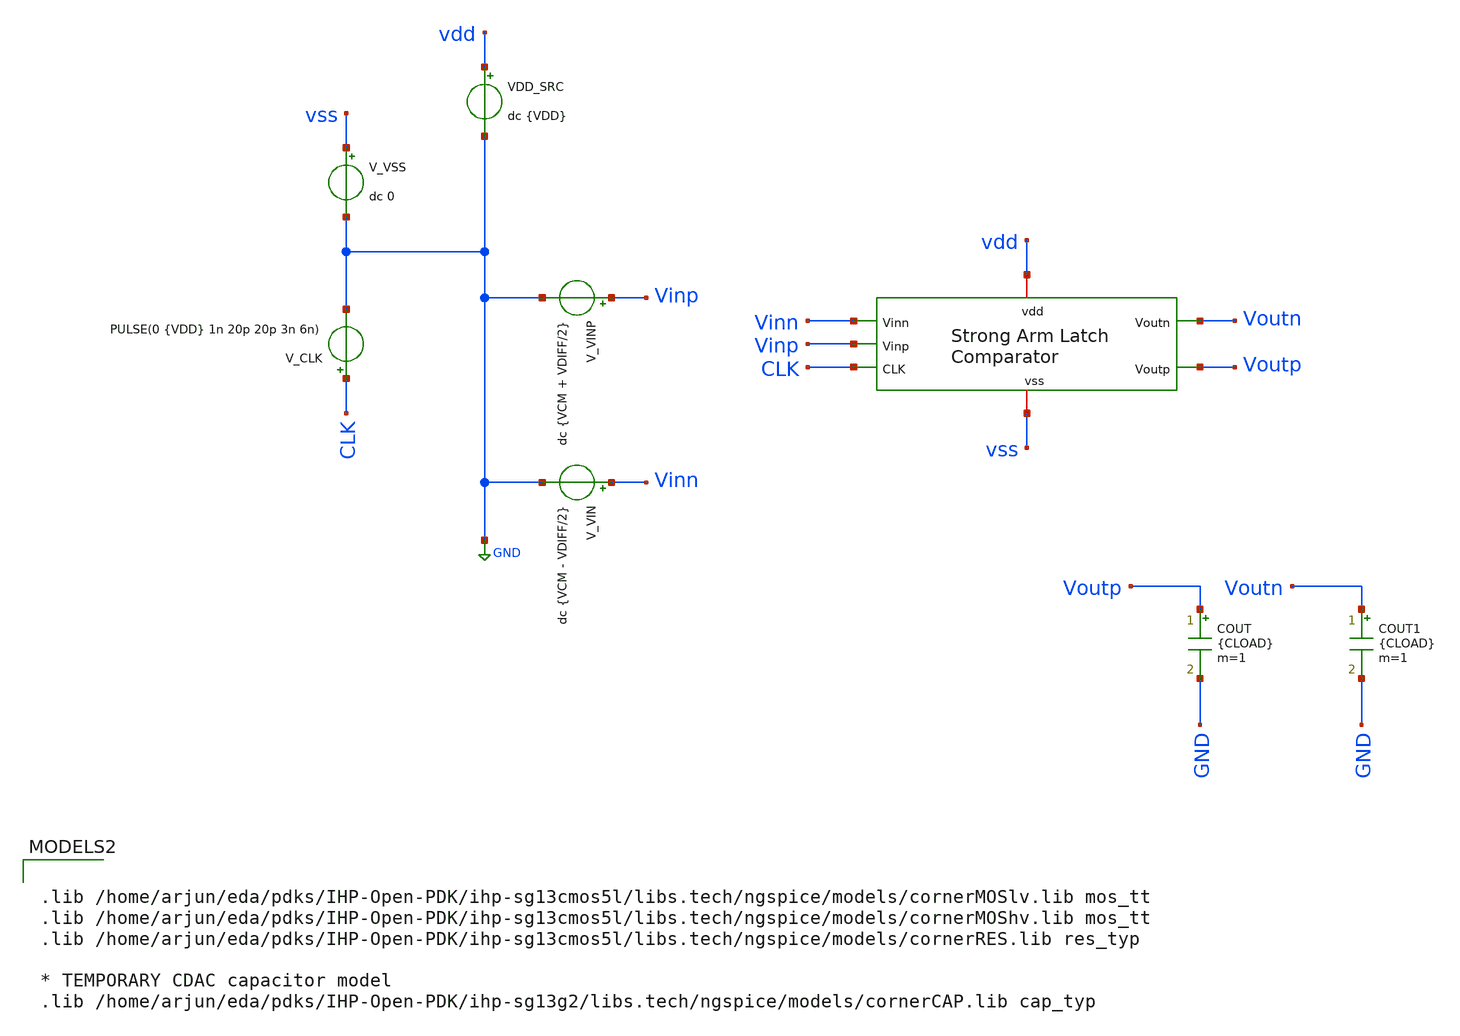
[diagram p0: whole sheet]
** sch_path: circuit_files/sar_adc_test/tb/strong_arm_comp_tb.sch
**.subckt strong_arm_comp_tb
V_VIN Vinn GND dc {VCM - VDIFF/2}
VDD_SRC vdd GND dc {VDD}
V_VINP Vinp GND dc {VCM + VDIFF/2}
V_VSS vss GND dc 0
V_CLK CLK GND PULSE(0 {VDD} 1n 20p 20p 3n 6n)
COUT Voutp GND {CLOAD} m=1
COUT1 Voutn GND {CLOAD} m=1
x1 Voutn Vinn Voutp Vinp vdd vss CLK strong_arm_comp
**** begin user architecture code



.param VDD=3.3
.param VCM=1.65
.param VREF=3.3
.param NBITS=10
.param VLSB=3.22265625e-3
.param VHLSB=1.611328125e-3
.param VDIFF=10e-3
.param CLOAD=20f

.options savecurrents
.options reltol=1e-4 abstol=1e-12 vntol=1e-6 method=gear

.save v(CLK) v(Vinp) v(Vinn) v(Voutp) v(Voutn)
.save v(x1.x) v(x1.y) v(x1.p) v(x1.q) v(x1.net1) v(x1.net2) v(x1.net3)
.save i(VDD_SRC)

.control
set filetype=binary

shell rm -f strongarm_results.txt
shell rm -f strongarm_tran_nominal.txt
shell rm -f strongarm_lsb_sweep.txt
shell rm -f strongarm_delay_sweep.txt
shell rm -f strongarm_vcm_sweep.txt
shell rm -f strongarm_vdd_sweep.txt

echo ============================================= > strongarm_results.txt
echo GF180MCU StrongARM comparator qualification >> strongarm_results.txt
echo For 10-bit SAR ADC check >> strongarm_results.txt
echo ============================================= >> strongarm_results.txt
echo . >> strongarm_results.txt
echo Assumed VREF = 3.3 V >> strongarm_results.txt
echo 10-bit LSB  = 3.22265625 mV >> strongarm_results.txt
echo 0.5 LSB     = 1.611328125 mV >> strongarm_results.txt
echo . >> strongarm_results.txt


alterparam VDD=3.3
alterparam VCM=1.65
alterparam VDIFF=10e-3
reset

op
tran 1p 5n
write strong_arm_comp_tb.raw

meas tran voutp_samp FIND v(Voutp) AT=4n
meas tran voutn_samp FIND v(Voutn) AT=4n
meas tran x_samp     FIND v(x1.x)     AT=4n
meas tran y_samp     FIND v(x1.y)     AT=4n
meas tran p_samp     FIND v(x1.p)     AT=4n
meas tran q_samp     FIND v(x1.q)     AT=4n
meas tran net1_samp  FIND v(x1.net1)  AT=4n
meas tran net2_samp  FIND v(x1.net2)  AT=4n
meas tran net3_samp  FIND v(x1.net3)  AT=4n

meas tran idd_avg    AVG i(VDD_SRC) FROM=0n TO=5n
meas tran idd_eval   AVG i(VDD_SRC) FROM=1n TO=4n

let vod_samp = voutp_samp - voutn_samp
let pavg = -3.3*idd_avg
let peval = -3.3*idd_eval
let e_5ns = pavg*5n
let e_eval = peval*3n

meas tran t_clk_rise WHEN v(CLK)=1.65 RISE=1
meas tran t_voutn_fall WHEN v(Voutn)=1.65 FALL=1
let td_pos = t_voutn_fall - t_clk_rise

echo ---- Nominal transient result, VDIFF = +10 mV ---- >> strongarm_results.txt
echo Voutp_4ns          = $&voutp_samp V >> strongarm_results.txt
echo Voutn_4ns          = $&voutn_samp V >> strongarm_results.txt
echo Voutp_minus_Voutn  = $&vod_samp   V >> strongarm_results.txt
echo X_4ns              = $&x_samp     V >> strongarm_results.txt
echo Y_4ns              = $&y_samp     V >> strongarm_results.txt
echo P_4ns              = $&p_samp     V >> strongarm_results.txt
echo Q_4ns              = $&q_samp     V >> strongarm_results.txt
echo net1_4ns           = $&net1_samp  V >> strongarm_results.txt
echo net2_4ns           = $&net2_samp  V >> strongarm_results.txt
echo net3_4ns           = $&net3_samp  V >> strongarm_results.txt
echo IDD_avg_0_to_5ns   = $&idd_avg    A >> strongarm_results.txt
echo Pavg_0_to_5ns      = $&pavg       W >> strongarm_results.txt
echo E_0_to_5ns         = $&e_5ns      J >> strongarm_results.txt
echo IDD_eval_1_to_4ns  = $&idd_eval   A >> strongarm_results.txt
echo Peval_1_to_4ns     = $&peval      W >> strongarm_results.txt
echo Eeval_1_to_4ns     = $&e_eval     J >> strongarm_results.txt
echo t_clk_rise         = $&t_clk_rise     s >> strongarm_results.txt
echo t_voutn_fall       = $&t_voutn_fall   s >> strongarm_results.txt
echo td_pos             = $&td_pos         s >> strongarm_results.txt
echo . >> strongarm_results.txt

wrdata strongarm_tran_nominal.txt time v(CLK) v(Vinp) v(Vinn) v(Voutp) v(Voutn) v(x1.x) v(x1.y)
+ v(x1.p) v(x1.q) v(x1.net1) v(x1.net2) v(x1.net3) i(VDD_SRC)

echo ============================================= > strongarm_lsb_sweep.txt
echo 10-bit SAR LSB decision sweep >> strongarm_lsb_sweep.txt
echo VREF = 3.3 V, LSB = 3.22265625 mV, 0.5LSB = 1.611328125 mV >> strongarm_lsb_sweep.txt
echo columns: VDIFF Voutp Voutn Vod X Y P Q net1 net2 net3 Pavg >> strongarm_lsb_sweep.txt
echo ============================================= >> strongarm_lsb_sweep.txt

foreach dv -10e-3 -5e-3 -3.22265625e-3 -1.611328125e-3 -1e-3 -500e-6 500e-6 1e-3 1.611328125e-3
+ 3.22265625e-3 5e-3 10e-3
  alterparam VDD=3.3
  alterparam VCM=1.65
  alterparam VDIFF=$dv
  reset
  tran 1p 5n

  meas tran vop FIND v(Voutp) AT=4n
  meas tran von FIND v(Voutn) AT=4n
  meas tran vx  FIND v(x1.x)     AT=4n
meas tran vy  FIND v(x1.y)     AT=4n
meas tran vp  FIND v(x1.p)     AT=4n
meas tran vq  FIND v(x1.q)     AT=4n
meas tran vn1 FIND v(x1.net1)  AT=4n
meas tran vn2 FIND v(x1.net2)  AT=4n
meas tran vn3 FIND v(x1.net3)  AT=4n
  meas tran ia  AVG i(VDD_SRC) FROM=0n TO=5n

  let vod = vop - von
  let ppwr = -3.3*ia

  echo $dv $&vop $&von $&vod $&vx $&vy $&vp $&vq $&vn1 $&vn2 $&vn3 $&ppwr >> strongarm_lsb_sweep.txt
end


echo ============================================= > strongarm_delay_sweep.txt
echo Delay versus positive VDIFF >> strongarm_delay_sweep.txt
echo columns: VDIFF tclk tout td Voutp4n Voutn4n Pavg >> strongarm_delay_sweep.txt
echo ============================================= >> strongarm_delay_sweep.txt

foreach dv 500e-6 1e-3 1.611328125e-3 3.22265625e-3 5e-3 10e-3 20e-3 50e-3
  alterparam VDD=3.3
  alterparam VCM=1.65
  alterparam VDIFF=$dv
  reset
  tran 1p 5n

  meas tran tclk WHEN v(CLK)=1.65 RISE=1
  meas tran tout WHEN v(Voutn)=1.65 FALL=1
  let td = tout - tclk

  meas tran vop4 FIND v(Voutp) AT=4n
  meas tran von4 FIND v(Voutn) AT=4n
  meas tran ia AVG i(VDD_SRC) FROM=0n TO=5n
  let ppwr = -3.3*ia

  echo $dv $&tclk $&tout $&td $&vop4 $&von4 $&ppwr >> strongarm_delay_sweep.txt
end

echo ============================================= > strongarm_vcm_sweep.txt
echo VCM sweep at VDIFF = +0.5 LSB >> strongarm_vcm_sweep.txt
echo columns: VCM Voutp4n Voutn4n Vod4n td Pavg >> strongarm_vcm_sweep.txt
echo ============================================= >> strongarm_vcm_sweep.txt

foreach cm 0.8 1.0 1.2 1.4 1.65 1.8 2.0 2.2 2.4
  alterparam VDD=3.3
  alterparam VCM=$cm
  alterparam VDIFF=1.611328125e-3
  reset
  tran 1p 5n

  meas tran vop4 FIND v(Voutp) AT=4n
  meas tran von4 FIND v(Voutn) AT=4n
  let vod4 = vop4 - von4

  meas tran tclk WHEN v(CLK)=1.65 RISE=1
  meas tran tout WHEN v(Voutn)=1.65 FALL=1
  let td = tout - tclk

  meas tran ia AVG i(VDD_SRC) FROM=0n TO=5n
  let ppwr = -3.3*ia

  echo $cm $&vop4 $&von4 $&vod4 $&td $&ppwr >> strongarm_vcm_sweep.txt
end


echo ============================================= > strongarm_vdd_sweep.txt
echo VDD sweep at VCM=VDD/2 and VDIFF=+0.5LSB >> strongarm_vdd_sweep.txt
echo columns: VDD VCM Voutp4n Voutn4n Vod4n td Pavg >> strongarm_vdd_sweep.txt
echo ============================================= >> strongarm_vdd_sweep.txt

* VDD = 3.0 V, VCM = 1.5 V
alterparam VDD=3.0
alterparam VCM=1.5
alterparam VDIFF=1.611328125e-3
reset
tran 1p 5n
meas tran vop4 FIND v(Voutp) AT=4n
meas tran von4 FIND v(Voutn) AT=4n
let vod4 = vop4 - von4
meas tran tclk WHEN v(CLK)=1.5 RISE=1
meas tran tout WHEN v(Voutn)=1.5 FALL=1
let td = tout - tclk
meas tran ia AVG i(VDD_SRC) FROM=0n TO=5n
let ppwr = -3.0*ia
echo 3.0 1.5 $&vop4 $&von4 $&vod4 $&td $&ppwr >> strongarm_vdd_sweep.txt

* VDD = 3.15 V, VCM = 1.575 V
alterparam VDD=3.15
alterparam VCM=1.575
alterparam VDIFF=1.611328125e-3
reset
tran 1p 5n
meas tran vop4 FIND v(Voutp) AT=4n
meas tran von4 FIND v(Voutn) AT=4n
let vod4 = vop4 - von4
meas tran tclk WHEN v(CLK)=1.575 RISE=1
meas tran tout WHEN v(Voutn)=1.575 FALL=1
let td = tout - tclk
meas tran ia AVG i(VDD_SRC) FROM=0n TO=5n
let ppwr = -3.15*ia
echo 3.15 1.575 $&vop4 $&von4 $&vod4 $&td $&ppwr >> strongarm_vdd_sweep.txt

* VDD = 3.3 V, VCM = 1.65 V
alterparam VDD=3.3
alterparam VCM=1.65
alterparam VDIFF=1.611328125e-3
reset
tran 1p 5n
meas tran vop4 FIND v(Voutp) AT=4n
meas tran von4 FIND v(Voutn) AT=4n
let vod4 = vop4 - von4
meas tran tclk WHEN v(CLK)=1.65 RISE=1
meas tran tout WHEN v(Voutn)=1.65 FALL=1
let td = tout - tclk
meas tran ia AVG i(VDD_SRC) FROM=0n TO=5n
let ppwr = -3.3*ia
echo 3.3 1.65 $&vop4 $&von4 $&vod4 $&td $&ppwr >> strongarm_vdd_sweep.txt

* VDD = 3.45 V, VCM = 1.725 V
alterparam VDD=3.45
alterparam VCM=1.725
alterparam VDIFF=1.611328125e-3
reset
tran 1p 5n
meas tran vop4 FIND v(Voutp) AT=4n
meas tran von4 FIND v(Voutn) AT=4n
let vod4 = vop4 - von4
meas tran tclk WHEN v(CLK)=1.725 RISE=1
meas tran tout WHEN v(Voutn)=1.725 FALL=1
let td = tout - tclk
meas tran ia AVG i(VDD_SRC) FROM=0n TO=5n
let ppwr = -3.45*ia
echo 3.45 1.725 $&vop4 $&von4 $&vod4 $&td $&ppwr >> strongarm_vdd_sweep.txt

* VDD = 3.6 V, VCM = 1.8 V
alterparam VDD=3.6
alterparam VCM=1.8
alterparam VDIFF=1.611328125e-3
reset
tran 1p 5n
meas tran vop4 FIND v(Voutp) AT=4n
meas tran von4 FIND v(Voutn) AT=4n
let vod4 = vop4 - von4
meas tran tclk WHEN v(CLK)=1.8 RISE=1
meas tran tout WHEN v(Voutn)=1.8 FALL=1
let td = tout - tclk
meas tran ia AVG i(VDD_SRC) FROM=0n TO=5n
let ppwr = -3.6*ia
echo 3.6 1.8 $&vop4 $&von4 $&vod4 $&td $&ppwr >> strongarm_vdd_sweep.txt

echo . >> strongarm_results.txt
echo Additional files generated: >> strongarm_results.txt
echo strongarm_lsb_sweep.txt >> strongarm_results.txt
echo strongarm_delay_sweep.txt >> strongarm_results.txt
echo strongarm_vcm_sweep.txt >> strongarm_results.txt
echo strongarm_vdd_sweep.txt >> strongarm_results.txt

echo Simulation complete.

.endc




.lib /home/arjun/eda/pdks/IHP-Open-PDK/ihp-sg13cmos5l/libs.tech/ngspice/models/cornerMOSlv.lib mos_tt
.lib /home/arjun/eda/pdks/IHP-Open-PDK/ihp-sg13cmos5l/libs.tech/ngspice/models/cornerMOShv.lib mos_tt
.lib /home/arjun/eda/pdks/IHP-Open-PDK/ihp-sg13cmos5l/libs.tech/ngspice/models/cornerRES.lib res_typ

* TEMPORARY CDAC capacitor model
.lib /home/arjun/eda/pdks/IHP-Open-PDK/ihp-sg13g2/libs.tech/ngspice/models/cornerCAP.lib cap_typ

**** end user architecture code
**.ends

* expanding   symbol:  strong_arm_comp.sym # of pins=7
** sym_path: circuit_files/sar_adc_test/xschem/strong_arm_comp.sym
** sch_path: circuit_files/sar_adc_test/xschem/strong_arm_comp.sch
.subckt strong_arm_comp Voutn Vinn Voutp Vinp vdd vss CLK
*.ipin Vinn
*.opin Voutp
*.iopin vdd
*.ipin Vinp
*.ipin CLK
*.iopin vss
*.opin Voutn
XM1 P CLK vdd vdd sg13_hv_pmos w=2u l=0.4u ng=1 m=4 mm_ok=1
XM2 net1 CLK vss vss sg13_hv_nmos w=2u l=0.45u ng=1 m=8 mm_ok=1
XM3 X CLK vdd vdd sg13_hv_pmos w=2u l=0.4u ng=1 m=4 mm_ok=1
XM4 P Vinn net1 vss sg13_hv_nmos w=2u l=0.45u ng=1 m=6 mm_ok=1
XM5 Q Vinp net1 vss sg13_hv_nmos w=2u l=0.45u ng=1 m=6 mm_ok=1
XM6 X Y P vss sg13_hv_nmos w=2u l=0.45u ng=1 m=2 mm_ok=1
XM7 Y X Q vss sg13_hv_nmos w=2u l=0.45u ng=1 m=2 mm_ok=1
XM8 X Y vdd vdd sg13_hv_pmos w=2u l=0.4u ng=1 m=4 mm_ok=1
XM9 Y CLK vdd vdd sg13_hv_pmos w=2u l=0.4u ng=1 m=4 mm_ok=1
XM10 Q CLK vdd vdd sg13_hv_pmos w=2u l=0.4u ng=1 m=4 mm_ok=1
XM11 Y X vdd vdd sg13_hv_pmos w=2u l=0.4u ng=1 m=4 mm_ok=1
XM12 net2 X vss vss sg13_hv_nmos w=2u l=0.45u ng=1 m=1 mm_ok=1
XM13 Voutp net2 vss vss sg13_hv_nmos w=2u l=0.45u ng=1 m=2 mm_ok=1
XM14 Voutn net3 vss vss sg13_hv_nmos w=2u l=0.45u ng=1 m=2 mm_ok=1
XM15 net3 Y vss vss sg13_hv_nmos w=2u l=0.45u ng=1 m=1 mm_ok=1
XM16 net2 X vdd vdd sg13_hv_pmos w=2u l=0.4u ng=1 m=2 mm_ok=1
XM17 Voutp Voutn vdd vdd sg13_hv_pmos w=2u l=0.4u ng=1 m=4 mm_ok=1
XM18 net3 Y vdd vdd sg13_hv_pmos w=2u l=0.4u ng=1 m=2 mm_ok=1
XM19 Voutn Voutp vdd vdd sg13_hv_pmos w=2u l=0.4u ng=1 m=4 mm_ok=1
.ends

.GLOBAL GND
.end
